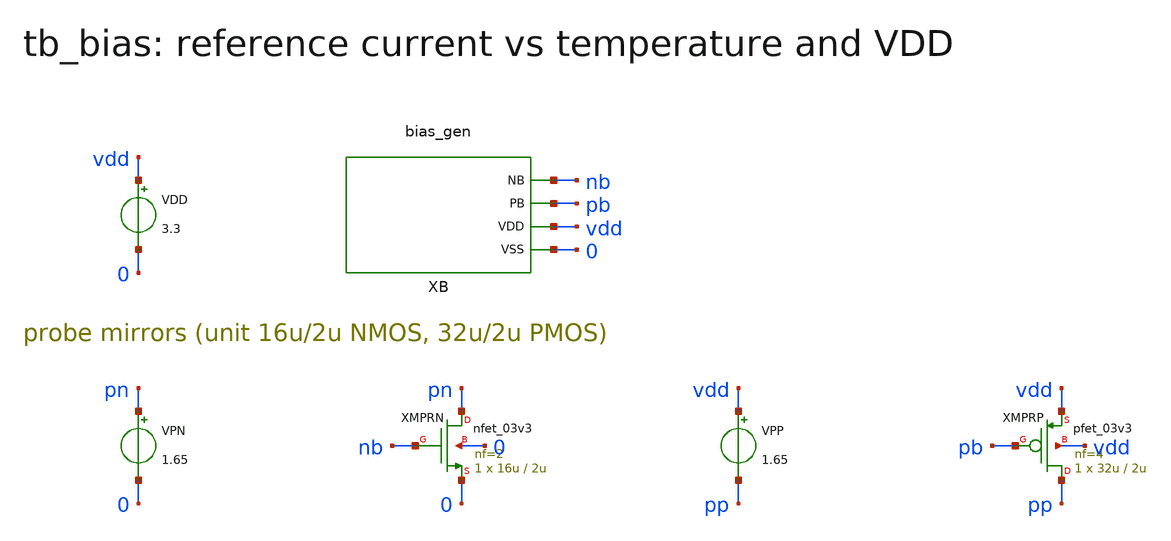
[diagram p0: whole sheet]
** sch_path: v1_claude/xschem/tb_bias.sch
**.subckt tb_bias
VDD vdd 0 3.3
XB nb pb vdd 0 bias_gen
VPN pn 0 1.65
XMPRN pn nb 0 0 nfet_03v3 L=2u W=16u nf=2 ad='int((nf+1)/2) * W/nf * 0.18u' as='int((nf+2)/2) * W/nf * 0.18u'
+ pd='2*int((nf+1)/2) * (W/nf + 0.18u)' ps='2*int((nf+2)/2) * (W/nf + 0.18u)' nrd='0.18u / W' nrs='0.18u / W'
+ sa=0 sb=0 sd=0 m=1
VPP vdd pp 1.65
XMPRP pp pb vdd vdd pfet_03v3 L=2u W=32u nf=4 ad='int((nf+1)/2) * W/nf * 0.18u' as='int((nf+2)/2) * W/nf * 0.18u'
+ pd='2*int((nf+1)/2) * (W/nf + 0.18u)' ps='2*int((nf+2)/2) * (W/nf + 0.18u)' nrd='0.18u / W' nrs='0.18u / W'
+ sa=0 sb=0 sd=0 m=1
**** begin user architecture code
 .include $::180MCU_MODELS/design.ngspice
.lib $::180MCU_MODELS/sm141064.ngspice typical
.lib $::180MCU_MODELS/sm141064.ngspice res_typical
.lib $::180MCU_MODELS/sm141064.ngspice mimcap_typical

.control
set num_threads=1
foreach tc -40 27 85 125
 set temp=$tc
 op
 echo RES temp=$tc in=$&@m.xmprn.m0[id] ip=$&@m.xmprp.m0[id] nb=$&v(nb) pb=$&v(pb)
end
set temp=27
dc VDD 2.8 3.6 0.2
print i(VPN)
.endc

**** end user architecture code
**.ends
.end
